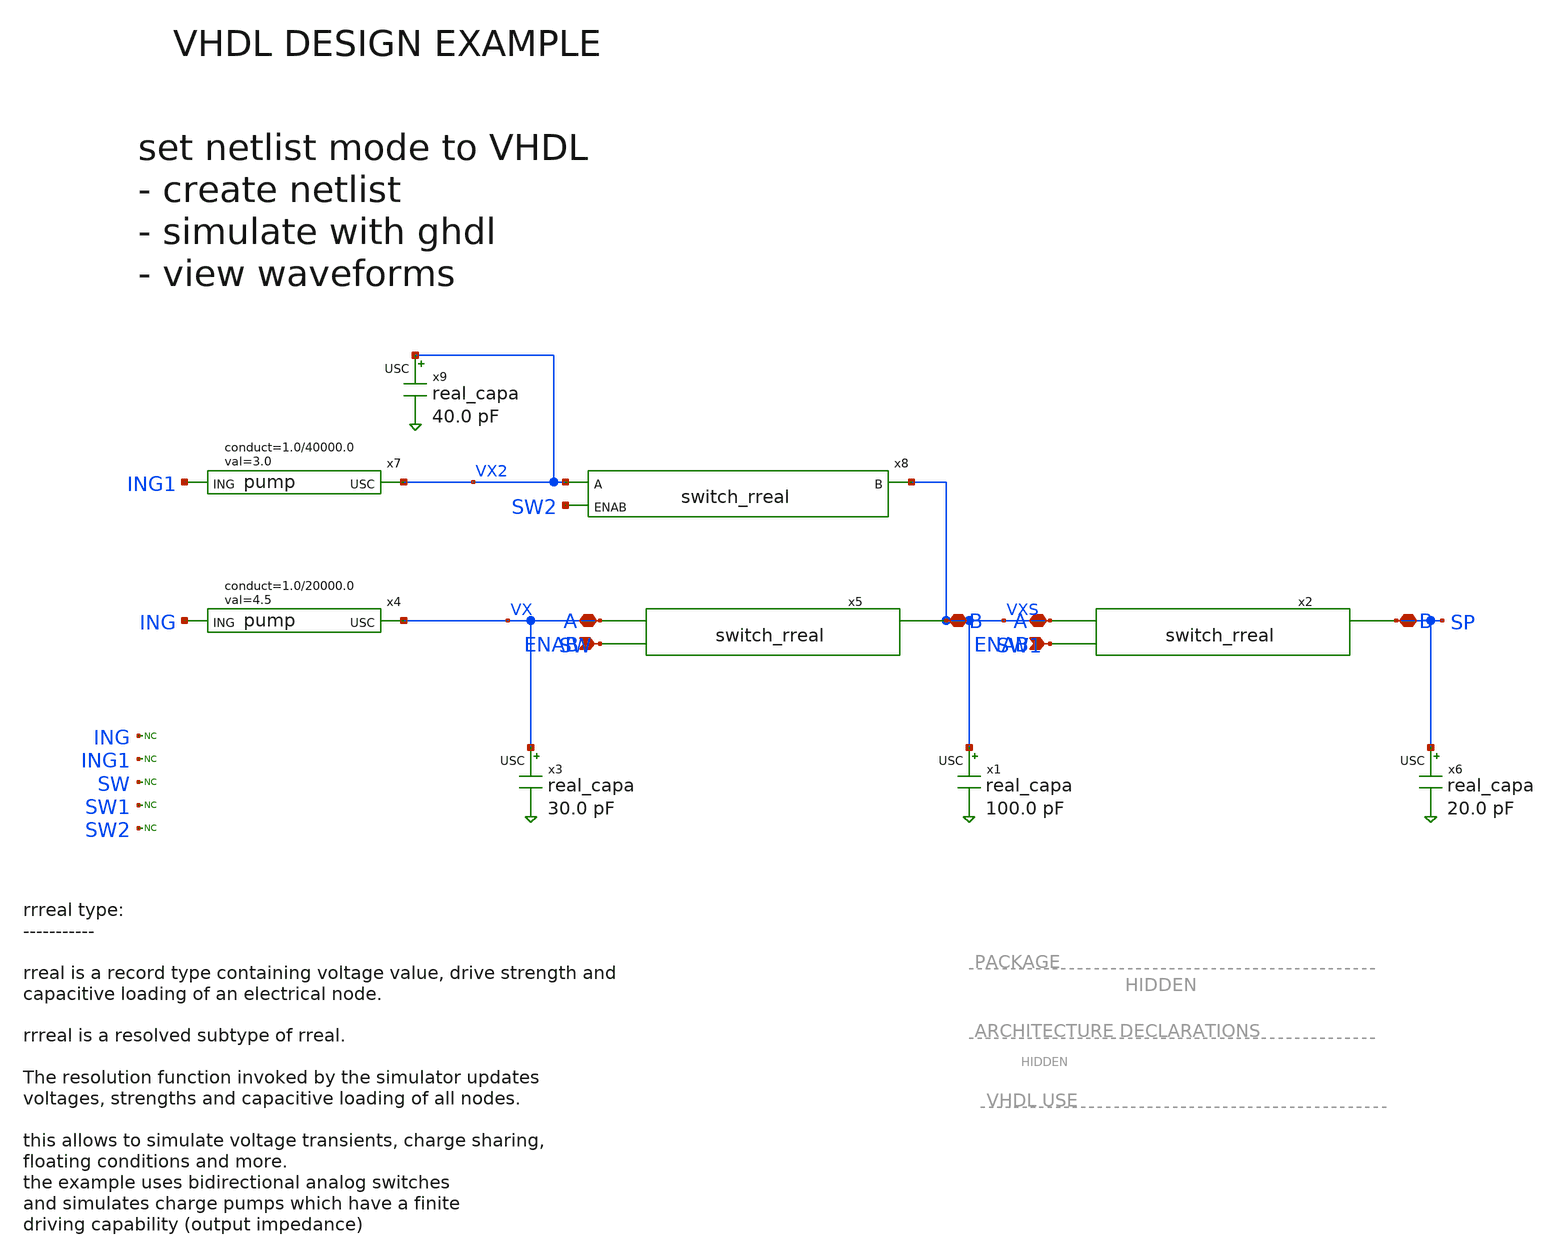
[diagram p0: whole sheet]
** sch_path: xschem-src/xschem_library/examples/loading.sch
* Copyright (C) 1998-2026 Stefan Frederik Schippers
* This program is free software; you can redistribute it and/or modify
* it under the terms of the GNU General Public License as published by
* the Free Software Foundation; either version 2 of the License, or
* (at your option) any later version.
* This program is distributed in the hope that it will be useful,
* but WITHOUT ANY WARRANTY; without even the implied warranty of
* MERCHANTABILITY or FITNESS FOR A PARTICULAR PURPOSE.  See the
* GNU General Public License for more details.
* You should have received a copy of the GNU General Public License
* along with this program; if not, write to the Free Software
**.subckt loading
x4 VX ING pump
x5 SW VXS VX switch_rreal
x3 VX real_capa
x1 VXS real_capa
x2 SW1 SP VXS switch_rreal
x6 SP real_capa
x7 VX2 ING1 pump
x8 SW2 VXS VX2 switch_rreal
x9 VX2 real_capa
* noconn ING
* noconn ING1
* noconn SW
* noconn SW1
* noconn SW2
**** begin user architecture code


-- these assignments are done to have the voltage values available
-- in the waveform file
V_VX <= VX.value;
V_VX2 <= VX2.value;
V_VXS <= VXS.value;
V_SP <= SP.value;


process
begin
ING<='0';
ING1<='0';
SW <= '0';
SW1<='0';
SW2<='0';
--VX <= rreal'(4.5,10.0,0.0);
--VX2 <= rreal'(3.0, 5.0, 0.0);
wait for 200 ns;
ING1<='1';
wait for 200 ns;
ING<='1';
wait for 200 ns;
SW<='1';
wait for 200 ns;
SW2<='1';
wait for 200 ns;
SW1<='1';
wait for 200 ns;
SW1<='0';
wait for 200 ns;
SW2<='0';
wait for 200 ns;
SW1<='1';
wait for 200 ns;
SW<='1';
wait for 200 ns;
ING <='0';
wait for 200 ns;
SW1<= '0';
wait for 200 ns;
SW<='1';
wait for 200 ns;
ING<='1';
wait for 200 ns;
SW <= '0';
wait for 200 ns;
SW1<= '1';
wait for 200 ns;
ING<='1';
wait for 200 ns;
SW<='0';
wait for 200 ns;
SW1<='0';
wait for 200 ns;
SW<='1';
wait for 200 ns;
SW1<='1';
wait for 200 ns;
SW1<='0';
wait for 200 ns;
SW1<='1';
wait for 200 ns;



wait;
end process;




* test
**** end user architecture code
**.ends

* expanding   symbol:  pump.sym # of pins=2
** sym_path: xschem-src/xschem_library/examples/pump.sym
** sch_path: xschem-src/xschem_library/examples/pump.sch
.subckt pump USC ING  val=4.5 conduct=10.0
*.iopin USC
*.ipin ING
.ends


* expanding   symbol:  switch_rreal.sch # of pins=3
** sym_path: xschem-src/xschem_library/examples/switch_rreal.sch
** sch_path: xschem-src/xschem_library/examples/switch_rreal.sch
.subckt switch_rreal ENAB B A  del=2 ns
*.ipin ENAB
*.iopin A
*.iopin B
.ends


* expanding   symbol:  real_capa.sym # of pins=1
** sym_path: xschem-src/xschem_library/examples/real_capa.sym
** sch_path: xschem-src/xschem_library/examples/real_capa.sch
.subckt real_capa USC  cap=10.0
*.iopin USC
.ends

.end
